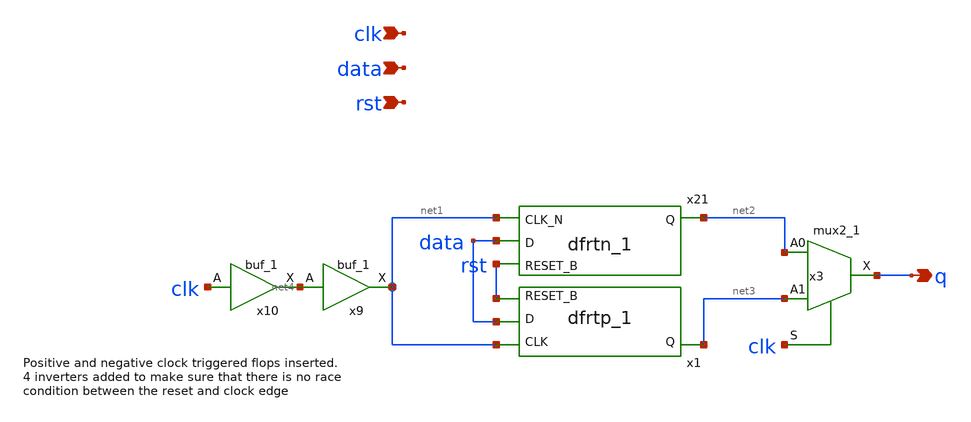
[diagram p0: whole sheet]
** sch_path: xschem/tryandtest/deff_rst.sch
**.subckt deff_rst clk data q rst
*.ipin clk
*.ipin data
*.opin q
*.ipin rst
x3 net2 net3 clk GND GND VDD VDD q sky130_fd_sc_lp__mux2_1
x21 net1 data rst GND GND VDD VDD net2 sky130_fd_sc_lp__dfrtn_1
x1 net1 data rst GND GND VDD VDD net3 sky130_fd_sc_lp__dfrtp_1
x9 net4 GND GND VDD VDD net1 sky130_fd_sc_lp__buf_1
x10 clk GND GND VDD VDD net4 sky130_fd_sc_lp__buf_1
**.ends
.end
